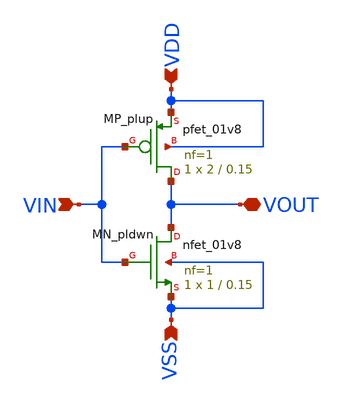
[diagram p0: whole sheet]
** sch_path: schem/symbol_repo/sym_inv.sch
**.subckt sym_inv VIN VDD VSS VOUT
*.ipin VIN
*.ipin VDD
*.ipin VSS
*.iopin VOUT
XMN_pldwn VOUT VIN VSS VSS sky130_fd_pr__nfet_01v8 L=0.15 W=1 nf=1 ad='int((1 + 1)/2) * 1 / 1 * 0.29'
+ as='int((1 + 2)/2) * 1 / 1 * 0.29' pd='2*int((1 + 1)/2) * (1 / 1 + 0.29)' ps='2*int((1 + 2)/2) * (1 / 1 + 0.29)'
+ nrd='0.29 / 1 ' nrs='0.29 / 1 ' sa=0 sb=0 sd=0 mult=1 m=1
XMP_plup VOUT VIN VDD VDD sky130_fd_pr__pfet_01v8 L=0.15 W=2 nf=1 ad='int((1 + 1)/2) * 2 / 1 * 0.29'
+ as='int((1 + 2)/2) * 2 / 1 * 0.29' pd='2*int((1 + 1)/2) * (2 / 1 + 0.29)' ps='2*int((1 + 2)/2) * (2 / 1 + 0.29)'
+ nrd='0.29 / 2 ' nrs='0.29 / 2 ' sa=0 sb=0 sd=0 mult=1 m=1
**.ends
.end
